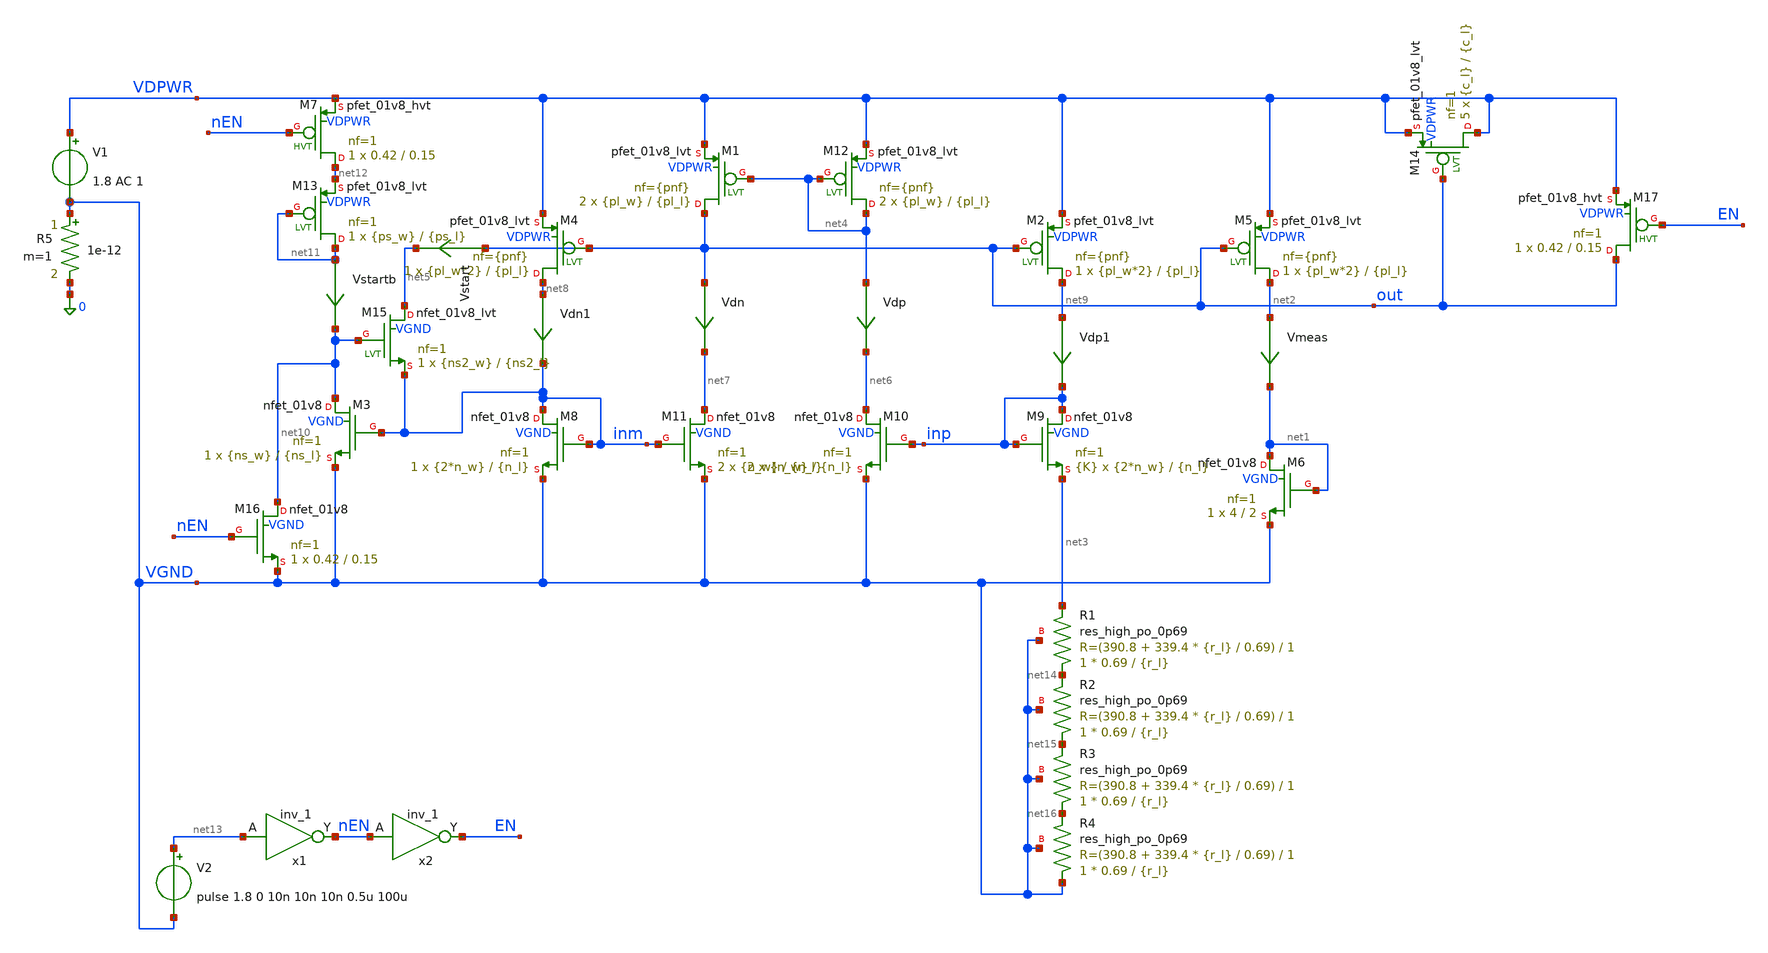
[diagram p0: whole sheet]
** sch_path: xschem/bias_testing.sch
**.subckt bias_testing
V1 VDPWR VGND 1.8 AC 1
XM4 net8 out VDPWR VDPWR sky130_fd_pr__pfet_01v8_lvt L={pl_l} W={pl_w*2} nf={pnf} ad='int(({pnf} + 1)/2) * {pl_w*2} / {pnf} * 0.29'
+ as='int(({pnf} + 2)/2) * {pl_w*2} / {pnf} * 0.29' pd='2*int(({pnf} + 1)/2) * ({pl_w*2} / {pnf} + 0.29)'
+ ps='2*int(({pnf} + 2)/2) * ({pl_w*2} / {pnf} + 0.29)' nrd='0.29 / {pl_w*2} ' nrs='0.29 / {pl_w*2} ' sa=0
+ sb=0 sd=0 mult=1 m=1
XM6 net1 net1 VGND VGND sky130_fd_pr__nfet_01v8 L=2 W=4 nf=1 ad='int((1 + 1)/2) * 4 / 1 * 0.29' as='int((1 + 2)/2) * 4 / 1 * 0.29'
+ pd='2*int((1 + 1)/2) * (4 / 1 + 0.29)' ps='2*int((1 + 2)/2) * (4 / 1 + 0.29)' nrd='0.29 / 4 ' nrs='0.29 / 4 '
+ sa=0 sb=0 sd=0 mult=1 m=1
Vmeas net2 net1 0
.save i(vmeas)
R5 VGND 0 1e-12 m=1
XM2 net9 out VDPWR VDPWR sky130_fd_pr__pfet_01v8_lvt L={pl_l} W={pl_w*2} nf={pnf} ad='int(({pnf} + 1)/2) * {pl_w*2} / {pnf} * 0.29'
+ as='int(({pnf} + 2)/2) * {pl_w*2} / {pnf} * 0.29' pd='2*int(({pnf} + 1)/2) * ({pl_w*2} / {pnf} + 0.29)'
+ ps='2*int(({pnf} + 2)/2) * ({pl_w*2} / {pnf} + 0.29)' nrd='0.29 / {pl_w*2} ' nrs='0.29 / {pl_w*2} ' sa=0
+ sb=0 sd=0 mult=1 m=1
XM5 net2 out VDPWR VDPWR sky130_fd_pr__pfet_01v8_lvt L={pl_l} W={pl_w*2} nf={pnf} ad='int(({pnf} + 1)/2) * {pl_w*2} / {pnf} * 0.29'
+ as='int(({pnf} + 2)/2) * {pl_w*2} / {pnf} * 0.29' pd='2*int(({pnf} + 1)/2) * ({pl_w*2} / {pnf} + 0.29)'
+ ps='2*int(({pnf} + 2)/2) * ({pl_w*2} / {pnf} + 0.29)' nrd='0.29 / {pl_w*2} ' nrs='0.29 / {pl_w*2} ' sa=0
+ sb=0 sd=0 mult=1 m=1
XM8 inm inm VGND VGND sky130_fd_pr__nfet_01v8 L={n_l} W={2*n_w} nf=1 ad='int((1 + 1)/2) * {2*n_w} / 1 * 0.29'
+ as='int((1 + 2)/2) * {2*n_w} / 1 * 0.29' pd='2*int((1 + 1)/2) * ({2*n_w} / 1 + 0.29)' ps='2*int((1 + 2)/2) * ({2*n_w} / 1 + 0.29)'
+ nrd='0.29 / {2*n_w} ' nrs='0.29 / {2*n_w} ' sa=0 sb=0 sd=0 mult=1 m=1
XM9 inp inp net3 VGND sky130_fd_pr__nfet_01v8 L={n_l} W={2*n_w} nf=1 ad='int((1 + 1)/2) * {2*n_w} / 1 * 0.29'
+ as='int((1 + 2)/2) * {2*n_w} / 1 * 0.29' pd='2*int((1 + 1)/2) * ({2*n_w} / 1 + 0.29)' ps='2*int((1 + 2)/2) * ({2*n_w} / 1 + 0.29)'
+ nrd='0.29 / {2*n_w} ' nrs='0.29 / {2*n_w} ' sa=0 sb=0 sd=0 mult={K} m={K}
XM10 net6 inp VGND VGND sky130_fd_pr__nfet_01v8 L={n_l} W={n_w} nf=1 ad='int((1 + 1)/2) * {n_w} / 1 * 0.29'
+ as='int((1 + 2)/2) * {n_w} / 1 * 0.29' pd='2*int((1 + 1)/2) * ({n_w} / 1 + 0.29)' ps='2*int((1 + 2)/2) * ({n_w} / 1 + 0.29)'
+ nrd='0.29 / {n_w} ' nrs='0.29 / {n_w} ' sa=0 sb=0 sd=0 mult=2 m=2
XM11 net7 inm VGND VGND sky130_fd_pr__nfet_01v8 L={n_l} W={n_w} nf=1 ad='int((1 + 1)/2) * {n_w} / 1 * 0.29'
+ as='int((1 + 2)/2) * {n_w} / 1 * 0.29' pd='2*int((1 + 1)/2) * ({n_w} / 1 + 0.29)' ps='2*int((1 + 2)/2) * ({n_w} / 1 + 0.29)'
+ nrd='0.29 / {n_w} ' nrs='0.29 / {n_w} ' sa=0 sb=0 sd=0 mult=2 m=2
XM15 net5 net10 inm VGND sky130_fd_pr__nfet_01v8_lvt L={ns2_l} W={ns2_w} nf=1 ad='int((1 + 1)/2) * {ns2_w} / 1 * 0.29'
+ as='int((1 + 2)/2) * {ns2_w} / 1 * 0.29' pd='2*int((1 + 1)/2) * ({ns2_w} / 1 + 0.29)' ps='2*int((1 + 2)/2) * ({ns2_w} / 1 + 0.29)'
+ nrd='0.29 / {ns2_w} ' nrs='0.29 / {ns2_w} ' sa=0 sb=0 sd=0 mult=1 m=1
XM3 net10 inm VGND VGND sky130_fd_pr__nfet_01v8 L={ns_l} W={ns_w} nf=1 ad='int((1 + 1)/2) * {ns_w} / 1 * 0.29'
+ as='int((1 + 2)/2) * {ns_w} / 1 * 0.29' pd='2*int((1 + 1)/2) * ({ns_w} / 1 + 0.29)' ps='2*int((1 + 2)/2) * ({ns_w} / 1 + 0.29)'
+ nrd='0.29 / {ns_w} ' nrs='0.29 / {ns_w} ' sa=0 sb=0 sd=0 mult=1 m=1
XR1 net14 net3 VGND sky130_fd_pr__res_high_po_0p69 L={r_l} mult=1 m=1
XR2 net15 net14 VGND sky130_fd_pr__res_high_po_0p69 L={r_l} mult=1 m=1
XR3 net16 net15 VGND sky130_fd_pr__res_high_po_0p69 L={r_l} mult=1 m=1
XR4 VGND net16 VGND sky130_fd_pr__res_high_po_0p69 L={r_l} mult=1 m=1
XM1 out net4 VDPWR VDPWR sky130_fd_pr__pfet_01v8_lvt L={pl_l} W={pl_w} nf={pnf} ad='int(({pnf} + 1)/2) * {pl_w} / {pnf} * 0.29'
+ as='int(({pnf} + 2)/2) * {pl_w} / {pnf} * 0.29' pd='2*int(({pnf} + 1)/2) * ({pl_w} / {pnf} + 0.29)' ps='2*int(({pnf} + 2)/2) * ({pl_w} / {pnf} + 0.29)'
+ nrd='0.29 / {pl_w} ' nrs='0.29 / {pl_w} ' sa=0 sb=0 sd=0 mult=2 m=2
XM12 net4 net4 VDPWR VDPWR sky130_fd_pr__pfet_01v8_lvt L={pl_l} W={pl_w} nf={pnf} ad='int(({pnf} + 1)/2) * {pl_w} / {pnf} * 0.29'
+ as='int(({pnf} + 2)/2) * {pl_w} / {pnf} * 0.29' pd='2*int(({pnf} + 1)/2) * ({pl_w} / {pnf} + 0.29)' ps='2*int(({pnf} + 2)/2) * ({pl_w} / {pnf} + 0.29)'
+ nrd='0.29 / {pl_w} ' nrs='0.29 / {pl_w} ' sa=0 sb=0 sd=0 mult=2 m=2
Vdn out net7 0
.save i(vdn)
Vdp net4 net6 0
.save i(vdp)
Vdn1 net8 inm 0
.save i(vdn1)
Vstartb net11 net10 0
.save i(vstartb)
Vdp1 net9 inp 0
.save i(vdp1)
Vstart out net5 0
.save i(vstart)
XM13 net11 net11 net12 VDPWR sky130_fd_pr__pfet_01v8_lvt L={ps_l} W={ps_w} nf=1 ad='int((1 + 1)/2) * {ps_w} / 1 * 0.29'
+ as='int((1 + 2)/2) * {ps_w} / 1 * 0.29' pd='2*int((1 + 1)/2) * ({ps_w} / 1 + 0.29)' ps='2*int((1 + 2)/2) * ({ps_w} / 1 + 0.29)'
+ nrd='0.29 / {ps_w} ' nrs='0.29 / {ps_w} ' sa=0 sb=0 sd=0 mult=1 m=1
XM16 net10 nEN VGND VGND sky130_fd_pr__nfet_01v8 L=0.15 W=0.42 nf=1 ad='int((1 + 1)/2) * 0.42 / 1 * 0.29'
+ as='int((1 + 2)/2) * 0.42 / 1 * 0.29' pd='2*int((1 + 1)/2) * (0.42 / 1 + 0.29)' ps='2*int((1 + 2)/2) * (0.42 / 1 + 0.29)'
+ nrd='0.29 / 0.42 ' nrs='0.29 / 0.42 ' sa=0 sb=0 sd=0 mult=1 m=1
x2 nEN VGND VGND VDPWR VDPWR EN sky130_fd_sc_hd__inv_1
V2 net13 VGND pulse 1.8 0 10n 10n 10n 0.5u 100u
XM17 out EN VDPWR VDPWR sky130_fd_pr__pfet_01v8_hvt L=0.15 W=0.42 nf=1 ad='int((1 + 1)/2) * 0.42 / 1 * 0.29'
+ as='int((1 + 2)/2) * 0.42 / 1 * 0.29' pd='2*int((1 + 1)/2) * (0.42 / 1 + 0.29)' ps='2*int((1 + 2)/2) * (0.42 / 1 + 0.29)'
+ nrd='0.29 / 0.42 ' nrs='0.29 / 0.42 ' sa=0 sb=0 sd=0 mult=1 m=1
XM7 net12 nEN VDPWR VDPWR sky130_fd_pr__pfet_01v8_hvt L=0.15 W=0.42 nf=1 ad='int((1 + 1)/2) * 0.42 / 1 * 0.29'
+ as='int((1 + 2)/2) * 0.42 / 1 * 0.29' pd='2*int((1 + 1)/2) * (0.42 / 1 + 0.29)' ps='2*int((1 + 2)/2) * (0.42 / 1 + 0.29)'
+ nrd='0.29 / 0.42 ' nrs='0.29 / 0.42 ' sa=0 sb=0 sd=0 mult=1 m=1
XM14 VDPWR out VDPWR VDPWR sky130_fd_pr__pfet_01v8_lvt L={c_l} W={c_l} nf=1 ad='int((1 + 1)/2) * {c_l} / 1 * 0.29'
+ as='int((1 + 2)/2) * {c_l} / 1 * 0.29' pd='2*int((1 + 1)/2) * ({c_l} / 1 + 0.29)' ps='2*int((1 + 2)/2) * ({c_l} / 1 + 0.29)'
+ nrd='0.29 / {c_l} ' nrs='0.29 / {c_l} ' sa=0 sb=0 sd=0 mult=5 m=5
x1 net13 VGND VGND VDPWR VDPWR nEN sky130_fd_sc_hd__inv_1
**** begin user architecture code


.param pl_w=2 pl_l=2 pnf=1 n_w=2 n_l=2 K=4 r_l=6.1
.param ns_w=0.5 ns_l=0.5 ns2_w=0.5 ns2_l=0.15 ps_l=3 ps_w=0.42 c_l=4
.save i(vmeas)
.options savecurrents
.save all
.control
let run = 0
dowhile run < 128
  dc TEMP -40 125 15 v1 1.6 2 0.2
*  plot i(vmeas)
  write reference.raw
  set appendwrite
  let run = run+1
  reset
end
.endc




.lib $::SKYWATER_MODELS/../ngspice/sky130.lib.spice tt_mm
.include $::SKYWATER_MODELS/../../libs.ref/sky130_fd_sc_hd/spice/sky130_fd_sc_hd.spice


**** end user architecture code
**.ends
.end
